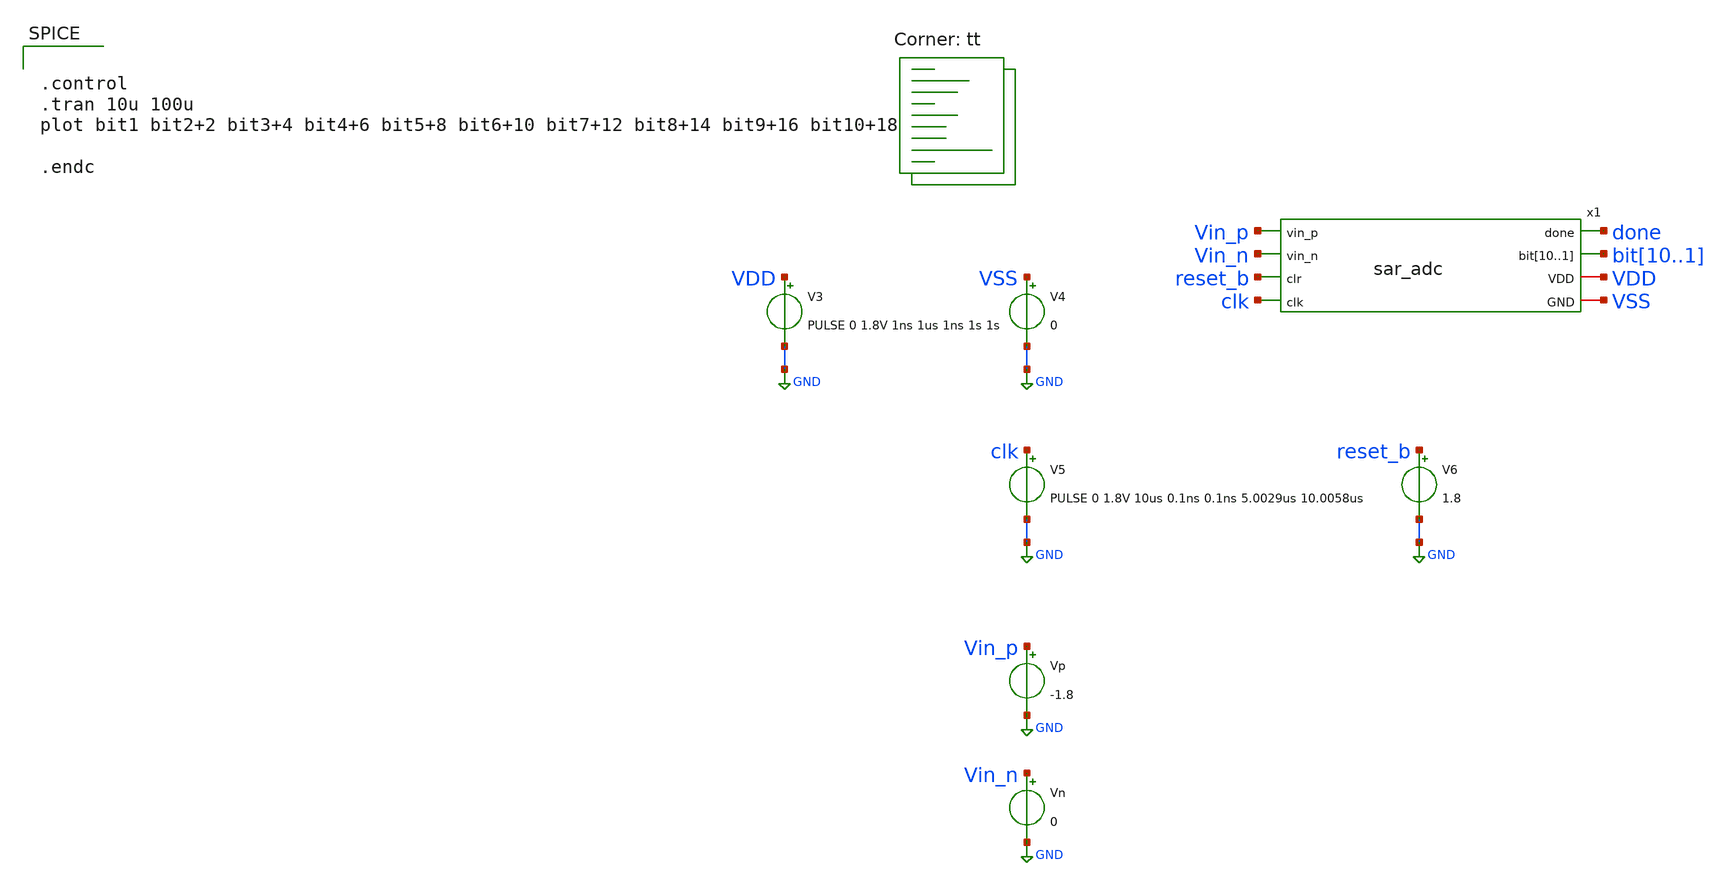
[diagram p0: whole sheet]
** sch_path: xschem/adc_test.sch
**.subckt adc_test
x1 done Vin_p bit10 bit9 bit8 bit7 bit6 bit5 bit4 bit3 bit2 bit1 Vin_n reset_b VDD clk VSS sar_adc
V3 VDD GND PULSE 0 1.8V 1ns 1us 1ns 1s 1s
V4 VSS GND 0
V5 clk GND PULSE 0 1.8V 10us 0.1ns 0.1ns 5.0029us 10.0058us
V6 reset_b GND 1.8
Vn Vin_n GND 0
Vp Vin_p GND -1.8
**** begin user architecture code
.lib $::SKYWATER_MODELS/sky130.lib.spice tt

*.lib $::SKYWATER_MODELS/sky130.lib.spice tt

* .lib $::SKYWATER_MODELS/sky130.lib.spice.tt.red tt

.include $::SKYWATER_STDCELLS/sky130_fd_sc_hd.spice



.control
.tran 10u 100u
plot bit1 bit2+2 bit3+4 bit4+6 bit5+8 bit6+10 bit7+12 bit8+14 bit9+16 bit10+18

.endc





.control
tran 10u 100u
plot bit1 bit2+2 bit3+4 bit4+6 bit5+8 bit6+10 bit7+12 bit8+14 bit9+16 bit10+18

.endc



**** end user architecture code
**.ends
.GLOBAL GND
.end
